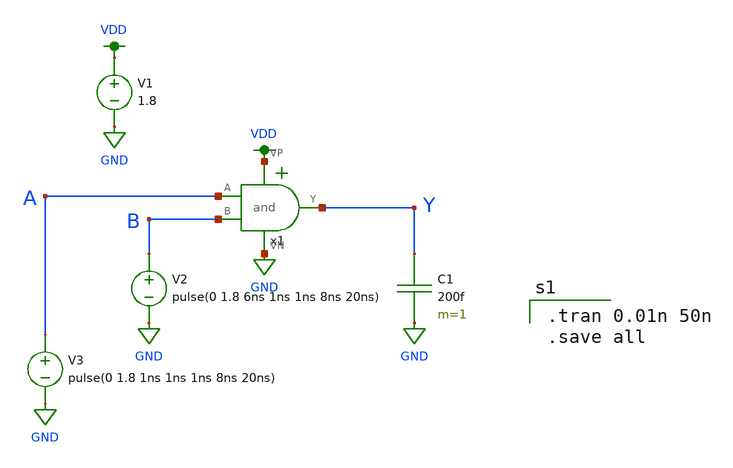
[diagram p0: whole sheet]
** sch_path: mp1/and/and_test.sch
**.subckt and_test
V1 VDD GND 1.8
V2 B GND pulse(0 1.8 6ns 1ns 1ns 8ns 20ns)
V3 A GND pulse(0 1.8 1ns 1ns 1ns 8ns 20ns)
x1 VDD A Y B GND and
C1 Y GND 200f m=1
**** begin user architecture code

.option wnflag=1
.lib ~/skywater/skywater-pdk/libraries/sky130_fd_pr_ngspice/latest/models/sky130.lib.spice tt


.tran 0.01n 50n
.save all

**** end user architecture code
**.ends

* expanding   symbol:  /home/madvlsi/dev/git/vlsi/mp1/and/and.sym # of pins=5
** sym_path: mp1/and/and.sym
** sch_path: mp1/and/and.sch
.subckt and VP A Y B VN
*.ipin A
*.ipin B
*.iopin VP
*.iopin VN
*.opin Y
x2 VP net1 A B VN nand
x1 VP net1 Y VN inverter
.ends


* expanding   symbol:  /home/madvlsi/dev/git/vlsi/mp1/and/nand.sym # of pins=5
** sym_path: mp1/and/nand.sym
** sch_path: mp1/and/nand.sch
.subckt nand VP Y A B VN
*.ipin A
*.ipin B
*.iopin VP
*.iopin VN
*.opin Y
XM1 net1 B VN VN sky130_fd_pr__nfet_01v8 L=0.15 W=1 nf=1 ad='int((nf+1)/2) * W/nf * 0.29' as='int((nf+2)/2) * W/nf * 0.29'
+ pd='2*int((nf+1)/2) * (W/nf + 0.29)' ps='2*int((nf+2)/2) * (W/nf + 0.29)' nrd='0.29 / W' nrs='0.29 / W'
+ sa=0 sb=0 sd=0 mult=1 m=1
XM2 Y A net1 VN sky130_fd_pr__nfet_01v8 L=0.15 W=1 nf=1 ad='int((nf+1)/2) * W/nf * 0.29' as='int((nf+2)/2) * W/nf * 0.29'
+ pd='2*int((nf+1)/2) * (W/nf + 0.29)' ps='2*int((nf+2)/2) * (W/nf + 0.29)' nrd='0.29 / W' nrs='0.29 / W'
+ sa=0 sb=0 sd=0 mult=1 m=1
XM3 Y A VP VP sky130_fd_pr__pfet_01v8 L=0.15 W=1 nf=1 ad='int((nf+1)/2) * W/nf * 0.29' as='int((nf+2)/2) * W/nf * 0.29'
+ pd='2*int((nf+1)/2) * (W/nf + 0.29)' ps='2*int((nf+2)/2) * (W/nf + 0.29)' nrd='0.29 / W' nrs='0.29 / W'
+ sa=0 sb=0 sd=0 mult=1 m=1
XM4 Y B VP VP sky130_fd_pr__pfet_01v8 L=0.15 W=1 nf=1 ad='int((nf+1)/2) * W/nf * 0.29' as='int((nf+2)/2) * W/nf * 0.29'
+ pd='2*int((nf+1)/2) * (W/nf + 0.29)' ps='2*int((nf+2)/2) * (W/nf + 0.29)' nrd='0.29 / W' nrs='0.29 / W'
+ sa=0 sb=0 sd=0 mult=1 m=1
.ends


* expanding   symbol:  /home/madvlsi/dev/git/vlsi/mp1/inverter/inverter.sym # of pins=4
** sym_path: mp1/inverter/inverter.sym
** sch_path: mp1/inverter/inverter.sch
.subckt inverter VP A Y VN
*.iopin VP
*.iopin VN
*.ipin A
*.opin Y
XM1 Y A VN VN sky130_fd_pr__nfet_01v8 L=0.15 W=1 nf=1 ad='int((nf+1)/2) * W/nf * 0.29' as='int((nf+2)/2) * W/nf * 0.29'
+ pd='2*int((nf+1)/2) * (W/nf + 0.29)' ps='2*int((nf+2)/2) * (W/nf + 0.29)' nrd='0.29 / W' nrs='0.29 / W'
+ sa=0 sb=0 sd=0 mult=1 m=1
XM2 Y A VP VP sky130_fd_pr__pfet_01v8 L=0.15 W=1 nf=1 ad='int((nf+1)/2) * W/nf * 0.29' as='int((nf+2)/2) * W/nf * 0.29'
+ pd='2*int((nf+1)/2) * (W/nf + 0.29)' ps='2*int((nf+2)/2) * (W/nf + 0.29)' nrd='0.29 / W' nrs='0.29 / W'
+ sa=0 sb=0 sd=0 mult=1 m=1
.ends

.GLOBAL VDD
.GLOBAL GND
.end
